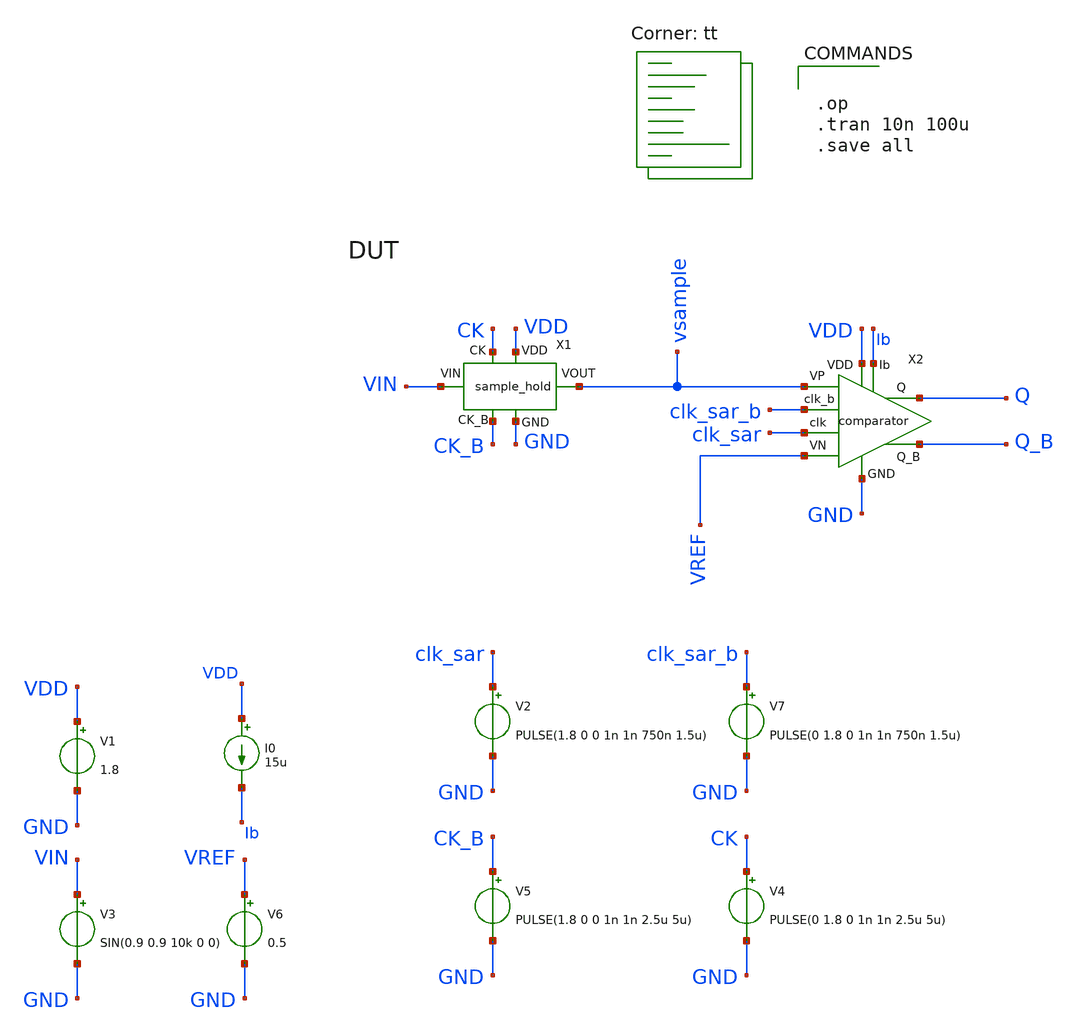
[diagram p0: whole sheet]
** sch_path: xschem/adc_top.sch
**.subckt adc_top
V1 VDD GND 1.8
V3 VIN GND SIN(0.9 0.9 10k 0 0)
V4 CK GND PULSE(0 1.8 0 1n 1n 2.5u 5u)
V5 CK_B GND PULSE(1.8 0 0 1n 1n 2.5u 5u)
V2 clk_sar GND PULSE(1.8 0 0 1n 1n 750n 1.5u)
V6 VREF GND 0.5
I0 VDD Ib 15u
X2 vsample VREF GND Q_B Q VDD clk_sar Ib clk_sar_b comparator
X1 GND VDD VIN vsample CK CK_B sample_hold
V7 clk_sar_b GND PULSE(0 1.8 0 1n 1n 750n 1.5u)
**** begin user architecture code
.lib $::SKYWATER_MODELS/sky130.lib.spice tt


.op
.tran 10n 100u
.save all


**** end user architecture code
**.ends
.end
